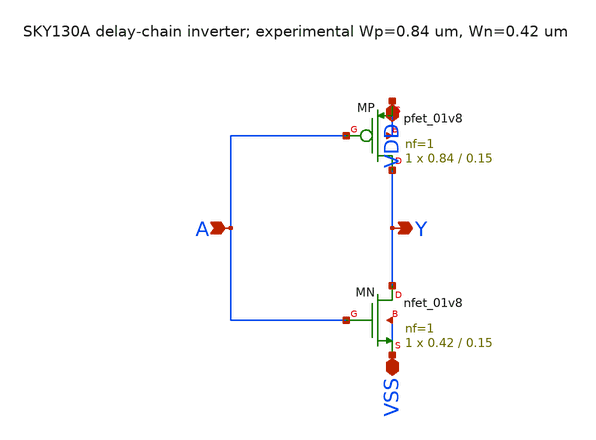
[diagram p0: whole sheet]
** sch_path: cells/control/phase_delay_inv.sch
**.subckt phase_delay_inv A Y VDD VSS
*.ipin A
*.opin Y
*.iopin VDD
*.iopin VSS
XMP Y A VDD VDD sky130_fd_pr__pfet_01v8 L=0.15 W=0.84 nf=1 ad='int((nf+1)/2) * W/nf * 0.29' as='int((nf+2)/2) * W/nf * 0.29'
+ pd='2*int((nf+1)/2) * (W/nf + 0.29)' ps='2*int((nf+2)/2) * (W/nf + 0.29)' nrd='0.29 / W' nrs='0.29 / W'
+ sa=0 sb=0 sd=0 mult=1 m=1
XMN Y A VSS VSS sky130_fd_pr__nfet_01v8 L=0.15 W=0.42 nf=1 ad='int((1 + 1)/2) * 0.42 / 1 * 0.29' as='int((1 + 2)/2) * 0.42 / 1 * 0.29'
+ pd='2*int((1 + 1)/2) * (0.42 / 1 + 0.29)' ps='2*int((1 + 2)/2) * (0.42 / 1 + 0.29)' nrd='0.29 / 0.42 '
+ nrs='0.29 / 0.42 ' sa=0 sb=0 sd=0 mult=1 m=1
**.ends
.end
